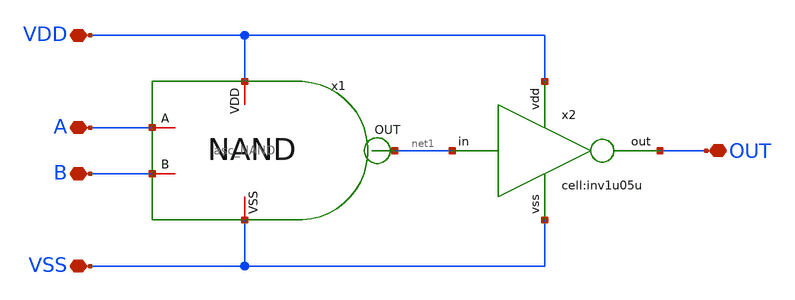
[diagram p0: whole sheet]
** sch_path: designs/libs/xp_core_analog/asc_AND/asc_AND.sch
**.subckt asc_AND VDD A B VSS OUT
*.iopin VDD
*.iopin A
*.iopin B
*.iopin VSS
*.iopin OUT
x1 VDD net1 A B VSS asc_NAND
x2 net1 VDD OUT VSS inv1u05u
**.ends
.end
